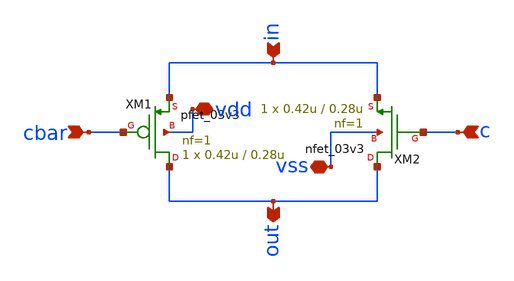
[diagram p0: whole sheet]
** sch_path: tgate.sch
**.subckt tgate in out cbar c vdd vss
*.ipin in
*.opin out
*.ipin cbar
*.ipin c
*.iopin vdd
*.iopin vss
XM1 out cbar in vdd pfet_03v3 L=0.28u W=0.42u nf=1 ad='int((nf+1)/2) * W/nf * 0.18u' as='int((nf+2)/2) * W/nf * 0.18u'
+ pd='2*int((nf+1)/2) * (W/nf + 0.18u)' ps='2*int((nf+2)/2) * (W/nf + 0.18u)' nrd='0.18u / W' nrs='0.18u / W'
+ sa=0 sb=0 sd=0 m=1
XM2 out c in vss nfet_03v3 L=0.28u W=0.42u nf=1 ad='int((nf+1)/2) * W/nf * 0.18u' as='int((nf+2)/2) * W/nf * 0.18u'
+ pd='2*int((nf+1)/2) * (W/nf + 0.18u)' ps='2*int((nf+2)/2) * (W/nf + 0.18u)' nrd='0.18u / W' nrs='0.18u / W'
+ sa=0 sb=0 sd=0 m=1
**.ends
.end
